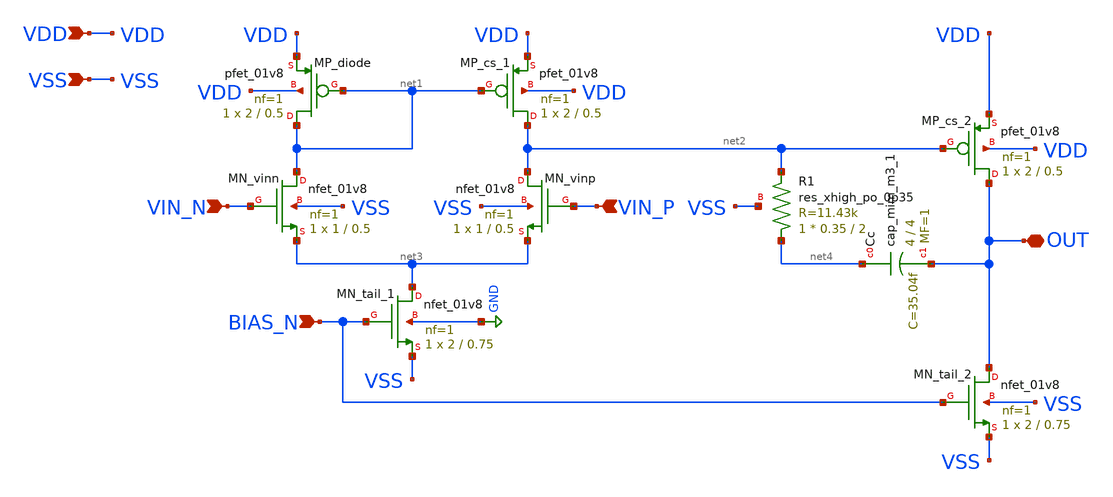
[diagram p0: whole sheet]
** sch_path: schem/symbol_repo/sym_opamp.sch
**.subckt sym_opamp VDD VSS BIAS_N OUT VIN_N VIN_P
*.ipin VDD
*.ipin VSS
*.ipin BIAS_N
*.iopin OUT
*.ipin VIN_N
*.ipin VIN_P
XMN_vinn net1 VIN_N net3 VSS sky130_fd_pr__nfet_01v8 L=0.5 W=1 nf=1 ad='int((1 + 1)/2) * 1 / 1 * 0.29'
+ as='int((1 + 2)/2) * 1 / 1 * 0.29' pd='2*int((1 + 1)/2) * (1 / 1 + 0.29)' ps='2*int((1 + 2)/2) * (1 / 1 + 0.29)'
+ nrd='0.29 / 1 ' nrs='0.29 / 1 ' sa=0 sb=0 sd=0 mult=1 m=1
XMP_cs_1 net2 net1 VDD VDD sky130_fd_pr__pfet_01v8 L=0.5 W=2 nf=1 ad='int((1 + 1)/2) * 2 / 1 * 0.29'
+ as='int((1 + 2)/2) * 2 / 1 * 0.29' pd='2*int((1 + 1)/2) * (2 / 1 + 0.29)' ps='2*int((1 + 2)/2) * (2 / 1 + 0.29)'
+ nrd='0.29 / 2 ' nrs='0.29 / 2 ' sa=0 sb=0 sd=0 mult=1 m=1
XMP_diode net1 net1 VDD VDD sky130_fd_pr__pfet_01v8 L=0.5 W=2 nf=1 ad='int((1 + 1)/2) * 2 / 1 * 0.29'
+ as='int((1 + 2)/2) * 2 / 1 * 0.29' pd='2*int((1 + 1)/2) * (2 / 1 + 0.29)' ps='2*int((1 + 2)/2) * (2 / 1 + 0.29)'
+ nrd='0.29 / 2 ' nrs='0.29 / 2 ' sa=0 sb=0 sd=0 mult=1 m=1
XMN_vinp net2 VIN_P net3 VSS sky130_fd_pr__nfet_01v8 L=0.5 W=1 nf=1 ad='int((1 + 1)/2) * 1 / 1 * 0.29'
+ as='int((1 + 2)/2) * 1 / 1 * 0.29' pd='2*int((1 + 1)/2) * (1 / 1 + 0.29)' ps='2*int((1 + 2)/2) * (1 / 1 + 0.29)'
+ nrd='0.29 / 1 ' nrs='0.29 / 1 ' sa=0 sb=0 sd=0 mult=1 m=1
XMN_tail_1 net3 BIAS_N VSS GND sky130_fd_pr__nfet_01v8 L=0.75 W=2 nf=1 ad='int((1 + 1)/2) * 2 / 1 * 0.29'
+ as='int((1 + 2)/2) * 2 / 1 * 0.29' pd='2*int((1 + 1)/2) * (2 / 1 + 0.29)' ps='2*int((1 + 2)/2) * (2 / 1 + 0.29)'
+ nrd='0.29 / 2 ' nrs='0.29 / 2 ' sa=0 sb=0 sd=0 mult=1 m=1
XMP_cs_2 OUT net2 VDD VDD sky130_fd_pr__pfet_01v8 L=0.5 W=2 nf=1 ad='int((1 + 1)/2) * 2 / 1 * 0.29' as='int((1 + 2)/2) * 2 / 1 * 0.29'
+ pd='2*int((1 + 1)/2) * (2 / 1 + 0.29)' ps='2*int((1 + 2)/2) * (2 / 1 + 0.29)' nrd='0.29 / 2 ' nrs='0.29 / 2 '
+ sa=0 sb=0 sd=0 mult=1 m=1
XMN_tail_2 OUT BIAS_N VSS VSS sky130_fd_pr__nfet_01v8 L=0.75 W=2 nf=1 ad='int((1 + 1)/2) * 2 / 1 * 0.29'
+ as='int((1 + 2)/2) * 2 / 1 * 0.29' pd='2*int((1 + 1)/2) * (2 / 1 + 0.29)' ps='2*int((1 + 2)/2) * (2 / 1 + 0.29)'
+ nrd='0.29 / 2 ' nrs='0.29 / 2 ' sa=0 sb=0 sd=0 mult=1 m=1
XCc net4 OUT sky130_fd_pr__cap_mim_m3_1 W=4 L=4 MF=1 m=1
XR1 net4 net2 VSS sky130_fd_pr__res_xhigh_po_0p35 L=2 mult=1 m=1
**.ends
.GLOBAL GND
.end
